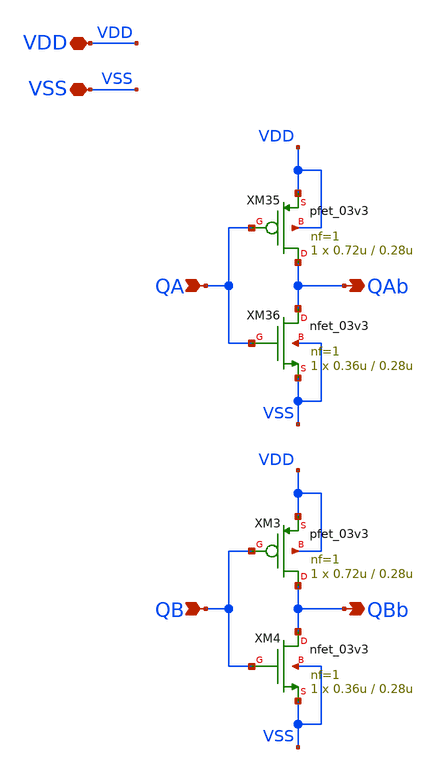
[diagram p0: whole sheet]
** sch_path: CAD3/output_inverter.sch
**.subckt output_inverter QBb QAb VDD VSS QA QB
*.opin QBb
*.opin QAb
*.iopin VDD
*.iopin VSS
*.ipin QA
*.ipin QB
XM3 QBb QB VDD VDD pfet_03v3 L=0.28u W=0.72u nf=1 ad='int((nf+1)/2) * W/nf * 0.18u' as='int((nf+2)/2) * W/nf * 0.18u'
+ pd='2*int((nf+1)/2) * (W/nf + 0.18u)' ps='2*int((nf+2)/2) * (W/nf + 0.18u)' nrd='0.18u / W' nrs='0.18u / W'
+ sa=0 sb=0 sd=0 m=1
XM4 QBb QB VSS VSS nfet_03v3 L=0.28u W=0.36u nf=1 ad='int((nf+1)/2) * W/nf * 0.18u' as='int((nf+2)/2) * W/nf * 0.18u'
+ pd='2*int((nf+1)/2) * (W/nf + 0.18u)' ps='2*int((nf+2)/2) * (W/nf + 0.18u)' nrd='0.18u / W' nrs='0.18u / W'
+ sa=0 sb=0 sd=0 m=1
XM35 QAb QA VDD VDD pfet_03v3 L=0.28u W=0.72u nf=1 ad='int((nf+1)/2) * W/nf * 0.18u' as='int((nf+2)/2) * W/nf * 0.18u'
+ pd='2*int((nf+1)/2) * (W/nf + 0.18u)' ps='2*int((nf+2)/2) * (W/nf + 0.18u)' nrd='0.18u / W' nrs='0.18u / W'
+ sa=0 sb=0 sd=0 m=1
XM36 QAb QA VSS VSS nfet_03v3 L=0.28u W=0.36u nf=1 ad='int((nf+1)/2) * W/nf * 0.18u' as='int((nf+2)/2) * W/nf * 0.18u'
+ pd='2*int((nf+1)/2) * (W/nf + 0.18u)' ps='2*int((nf+2)/2) * (W/nf + 0.18u)' nrd='0.18u / W' nrs='0.18u / W'
+ sa=0 sb=0 sd=0 m=1
**.ends
.end
